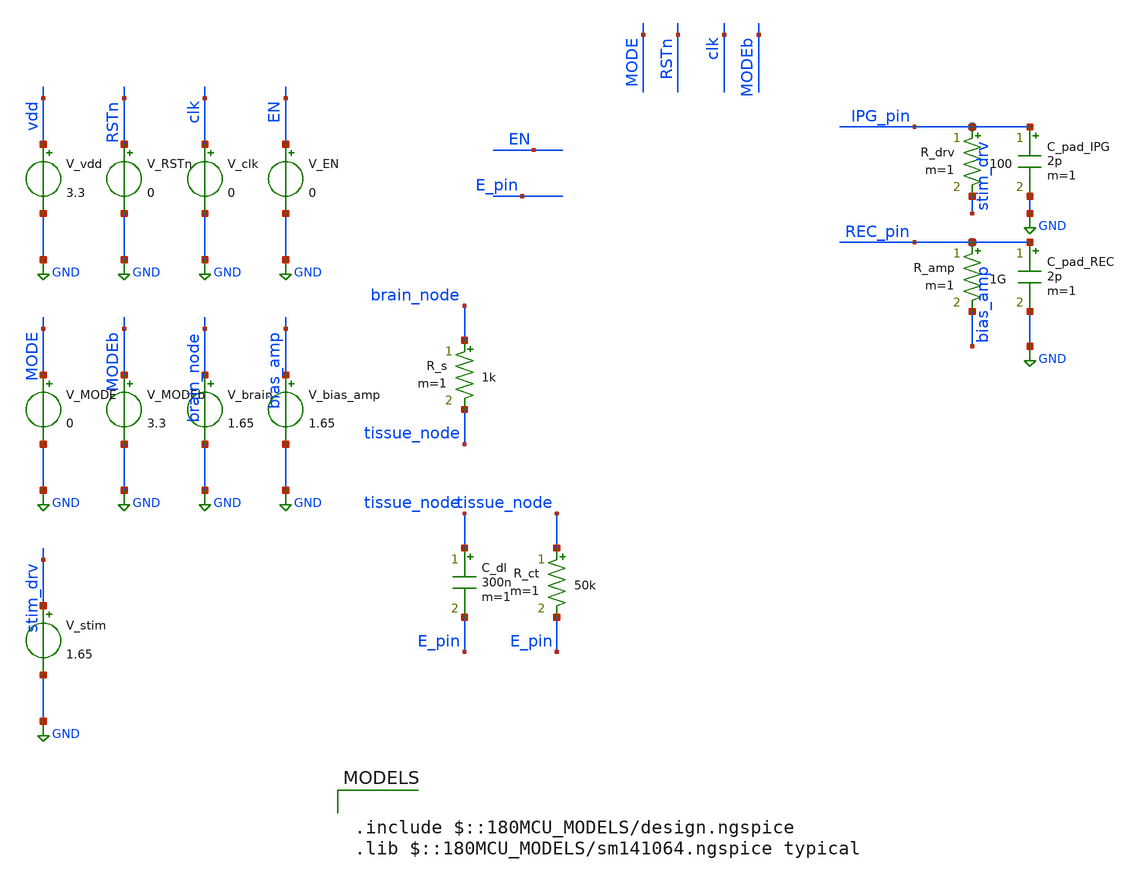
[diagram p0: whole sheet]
** sch_path: tb_realistic_postpex.sch
**.subckt tb_realistic_postpex
V_vdd vdd GND 3.3
V_RSTn RSTn GND 0
V_clk clk GND 0
V_EN EN GND 0
V_MODE MODE GND 0
V_MODEb MODEb GND 3.3
V_brain brain_node GND 1.65
V_bias_amp bias_amp GND 1.65
V_stim stim_drv GND 1.65
R_s brain_node tissue_node 1k m=1
R_ct tissue_node E_pin 50k m=1
C_dl tissue_node E_pin 300n m=1
R_drv IPG_pin stim_drv 100 m=1
C_pad_IPG IPG_pin GND 2p m=1
R_amp REC_pin bias_amp 1G m=1
C_pad_REC REC_pin GND 2p m=1
**** begin user architecture code

.include $::180MCU_MODELS/design.ngspice
.lib $::180MCU_MODELS/sm141064.ngspice typical



.SUBCKT ROW VDD E REC RSTn EN CLK MODE GND IPG MODEb
M1 n8 n7 VDD VDD pfet_03v3 L=0.28U W=1U AS=0.65P AD=0.42P PS=3.3U PD=1.84U
M2 VDD n20 n8 VDD pfet_03v3 L=0.28U W=1U AS=0.42P AD=0.735P PS=1.84U PD=2.47U
M3 n9 n8 VDD VDD pfet_03v3 L=0.28U W=1U AS=0.735P AD=0.635P PS=2.47U PD=3.27U
M4 n10 n9 VDD VDD pfet_03v3 L=0.28U W=1U AS=0.55P AD=0.65P PS=3.1U PD=3.3U
M5 REC n10 E VDD pfet_03v3 L=0.28U W=1U AS=0.65P AD=0.65P PS=3.3U PD=3.3U
M6 n3 n13 VDD VDD pfet_03v3 L=0.28U W=1U AS=0.76P AD=0.65P PS=3.52U PD=3.3U
M7 VDD n3 n4 VDD pfet_03v3 L=0.28U W=1U AS=0.65P AD=0.65P PS=3.3U PD=3.3U
M8 n4 RSTn VDD VDD pfet_03v3 L=0.28U W=1U AS=0.65P AD=0.65P PS=3.3U PD=3.3U
M9 n13 n2 n4 VDD pfet_03v3 L=0.28U W=1U AS=0.65P AD=0.59P PS=3.3U PD=3.18U
M10 n5 EN n13 VDD pfet_03v3 L=0.28U W=1U AS=0.63P AD=0.605P PS=3.26U PD=3.21U
M11 VDD n15 n5 VDD pfet_03v3 L=0.28U W=1U AS=0.63P AD=0.54P PS=3.26U PD=3.08U
M12 VDD n2 n15 VDD pfet_03v3 L=0.28U W=1U AS=0.63P AD=0.64P PS=3.26U PD=3.28U
M13 VDD CLK n2 VDD pfet_03v3 L=0.28U W=1U AS=0.65P AD=0.65P PS=3.3U PD=3.3U
M14 n6 MODE VDD VDD pfet_03v3 L=0.28U W=1U AS=0.65P AD=0.42P PS=3.3U PD=1.84U
M15 VDD n18 n6 VDD pfet_03v3 L=0.28U W=1U AS=0.42P AD=0.735P PS=1.84U  PD=2.47U
M16 n7 n6 VDD VDD pfet_03v3 L=0.28U W=1U AS=0.735P AD=0.64P PS=2.47U PD=3.28U
M17 n56 n54 VDD VDD pfet_03v3 L=0.28U W=1U AS=0.65P AD=0.65P PS=3.3U PD=3.3U
M18 n85 n56 n54 VDD pfet_03v3 L=0.28U W=1U AS=0.65P AD=0.65P PS=3.3U PD=3.3U
M19 VDD n15 n85 VDD pfet_03v3 L=0.28U W=1U AS=0.65P AD=0.65P PS=3.3U PD=3.3U
M20 n18 n56 VDD VDD pfet_03v3 L=0.28U W=1U AS=0.65P AD=0.65P PS=3.3U PD=3.3U
M21 n58 n56 VDD VDD pfet_03v3 L=0.28U W=1U AS=0.65P AD=0.65P PS=3.3U PD=3.3U
M22 n59 n58 VDD VDD pfet_03v3 L=0.28U W=1U AS=0.65P AD=0.65P PS=3.3U PD=3.3U
M23 n60 MODEb VDD VDD pfet_03v3 L=0.28U W=1U AS=0.65P AD=0.42P PS=3.3U  PD=1.84U
M24 VDD n18 n60 VDD pfet_03v3 L=0.28U W=1U AS=0.42P AD=0.735P PS=1.84U  PD=2.47U
M25 n67 n60 VDD VDD pfet_03v3 L=0.28U W=1U AS=0.735P AD=0.63P PS=2.47U  PD=3.26U
M26 n54 n2 n3 VDD pfet_03v3 L=0.28U W=1U AS=0.65P AD=0.65P PS=3.3U PD=3.3U
M27 n56 RSTn VDD VDD pfet_03v3 L=0.28U W=1U AS=0.65P AD=0.65P PS=3.3U PD=3.3U
M28 n61 n67 VDD VDD pfet_03v3 L=0.28U W=1U AS=0.65P AD=0.42P PS=3.3U PD=1.84U
M29 VDD n10 n61 VDD pfet_03v3 L=0.28U W=1U AS=0.42P AD=0.735P PS=1.84U  PD=2.47U
M30 n68 n61 VDD VDD pfet_03v3 L=0.28U W=1U AS=0.735P AD=0.63P PS=2.47U  PD=3.26U
M31 n20 n68 VDD VDD pfet_03v3 L=0.28U W=1U AS=0.56P AD=0.65P PS=3.12U PD=3.3U
M32 IPG n20 E VDD pfet_03v3 L=0.28U W=1U AS=0.65P AD=0.65P PS=3.3U PD=3.3U
M33 n9 n8 GND GND nfet_03v3 L=0.28U W=0.5U AS=0.2425P AD=0.315P PS=1.97U  PD=2.26U
M34 n10 n9 GND GND nfet_03v3 L=0.28U W=0.5U AS=0.2825P AD=0.315P PS=2.13U  PD=2.26U
M35 n7 n6 GND GND nfet_03v3 L=0.28U W=0.5U AS=0.2425P AD=0.3125P PS=1.97U  PD=2.25U
M36 n52 n7 GND GND nfet_03v3 L=0.28U W=1U AS=0.63P AD=0.42P PS=3.26U PD=1.84U
M37 n8 n20 n52 GND nfet_03v3 L=0.28U W=1U AS=0.42P AD=0.65P PS=1.84U PD=3.3U
M38 REC n9 E GND nfet_03v3 L=0.28U W=1U AS=0.63P AD=0.63P PS=3.26U PD=3.26U
M39 n3 n13 GND GND nfet_03v3 L=0.28U W=1U AS=0.76P AD=0.61P PS=3.52U PD=3.22U
M40 n34 n3 GND GND nfet_03v3 L=0.28U W=1U AS=0.61P AD=0.61P PS=3.22U PD=3.22U
M41 n4 RSTn n34 GND nfet_03v3 L=0.28U W=1U AS=0.61P AD=0.61P PS=3.22U  PD=3.22U
M42 n13 n15 n4 GND nfet_03v3 L=0.28U W=1U AS=0.61P AD=0.61P PS=3.22U  PD=3.22U
M43 n35 EN n13 GND nfet_03v3 L=0.28U W=1U AS=0.61P AD=0.61P PS=3.22U PD=3.22U
M44 GND n2 n35 GND nfet_03v3 L=0.28U W=1U AS=0.61P AD=0.575P PS=3.22U  PD=3.15U
M45 GND n2 n15 GND nfet_03v3 L=0.28U W=1U AS=0.61P AD=0.61P PS=3.22U PD=3.22U
M46 GND CLK n2 GND nfet_03v3 L=0.28U W=1U AS=0.63P AD=0.67P PS=3.26U PD=3.34U
M47 n47 MODE GND GND nfet_03v3 L=0.28U W=1U AS=0.63P AD=0.42P PS=3.26U  PD=1.84U
M48 n6 n18 n47 GND nfet_03v3 L=0.28U W=1U AS=0.42P AD=0.65P PS=1.84U PD=3.3U
M49 n54 n15 n3 GND nfet_03v3 L=0.28U W=1U AS=0.715P AD=0.61P PS=3.43U  PD=3.22U
M50 n55 RSTn GND GND nfet_03v3 L=0.28U W=1U AS=0.61P AD=0.61P PS=3.22U  PD=3.22U
M51 n56 n54 n55 GND nfet_03v3 L=0.28U W=1U AS=0.61P AD=0.61P PS=3.22U  PD=3.22U
M52 n57 n56 n54 GND nfet_03v3 L=0.28U W=1U AS=0.61P AD=0.61P PS=3.22U  PD=3.22U
M53 GND n2 n57 GND nfet_03v3 L=0.28U W=1U AS=0.61P AD=0.61P PS=3.22U PD=3.22U
M54 n18 n56 GND GND nfet_03v3 L=0.28U W=1U AS=0.61P AD=0.61P PS=3.22U  PD=3.22U
M55 n58 n56 GND GND nfet_03v3 L=0.28U W=1U AS=0.61P AD=0.61P PS=3.22U  PD=3.22U
M56 n59 n58 GND GND nfet_03v3 L=0.28U W=1U AS=0.61P AD=0.61P PS=3.22U  PD=3.22U
M57 n81 MODEb GND GND nfet_03v3 L=0.28U W=1U AS=0.63P AD=0.42P PS=3.26U  PD=1.84U
M58 n60 n18 n81 GND nfet_03v3 L=0.28U W=1U AS=0.42P AD=0.65P PS=1.84U  PD=3.3U
M59 n67 n60 GND GND nfet_03v3 L=0.28U W=0.5U AS=0.2425P AD=0.31P PS=1.97U  PD=2.24U
M60 n82 n67 GND GND nfet_03v3 L=0.28U W=1U AS=0.63P AD=0.42P PS=3.26U  PD=1.84U
M61 n61 n10 n82 GND nfet_03v3 L=0.28U W=1U AS=0.42P AD=0.65P PS=1.84U  PD=3.3U
M62 n68 n61 GND GND nfet_03v3 L=0.28U W=0.5U AS=0.2425P AD=0.3275P PS=1.97U  PD=2.31U
M63 n20 n68 GND GND nfet_03v3 L=0.28U W=0.5U AS=0.285P AD=0.315P PS=2.14U  PD=2.26U
M64 IPG n68 E GND nfet_03v3 L=0.28U W=1U AS=0.63P AD=0.63P PS=3.26U PD=3.26U
.ENDS ROW

X0 vdd E_pin REC_pin RSTn EN clk MODE GND IPG_pin MODEb ROW




.control
save all

** RSTn: low until 100ns then high
alter @V_RSTn[PWL] = [ 0 0  100n 0  100.001n 3.3  30m 3.3 ]

** Single latching clock pulse around 200ns
alter @V_clk[PWL] = [ 0 0  200n 0  200.001n 3.3  300n 3.3  300.001n 0  30m 0 ]

** EN: high after RSTn release
alter @V_EN[PWL] = [ 0 0  150n 0  150.001n 3.3  30m 3.3 ]

** MODE: stim phase 0-15ms (includes drain), record phase 15-30ms
alter @V_MODE[PWL]  = [ 0 0    15m 0    15.0001m 3.3   30m 3.3 ]
alter @V_MODEb[PWL] = [ 0 3.3  15m 3.3  15.0001m 0     30m 0 ]

** Brain LFP: 100uV sine at 1kHz on 1.65V mid-rail
alter @V_brain[SIN] = [ 1.65 10m 1k 0 0 0 ]

** Stim driver: biphasic pulses at 0.5/1.5/2.5/3.5/4.5 ms during stim phase,
** then held at mid-rail for 10 ms drain before MODE switches.
alter @V_stim[PWL] = [  0          1.65  500u       1.65  500.001u   0.65  600u       0.65  600.001u
+   2.65  700u       2.65  700.001u   1.65  1500u      1.65  1500.001u  0.65  1600u      0.65  1600.001u
+  2.65  1700u      2.65  1700.001u  1.65  2500u      1.65  2500.001u  0.65  2600u      0.65  2600.001u
+  2.65  2700u      2.65  2700.001u  1.65  3500u      1.65  3500.001u  0.65  3600u      0.65  3600.001u
+  2.65  3700u      2.65  3700.001u  1.65  4500u      1.65  4500.001u  0.65  4600u      0.65  4600.001u
+  2.65  4700u      2.65  4700.001u  1.65  30m        1.65 ]

tran 1u 30m 0 5u

** plots
set color0 = white
plot (v(MODE)/6.6)+1.4 v(REC_pin) v(E_pin) v(IPG_pin)/3 + (1.65-1.65/3)

write tb_realistic.raw
.endc


**** end user architecture code
**.ends
.GLOBAL GND
.end
